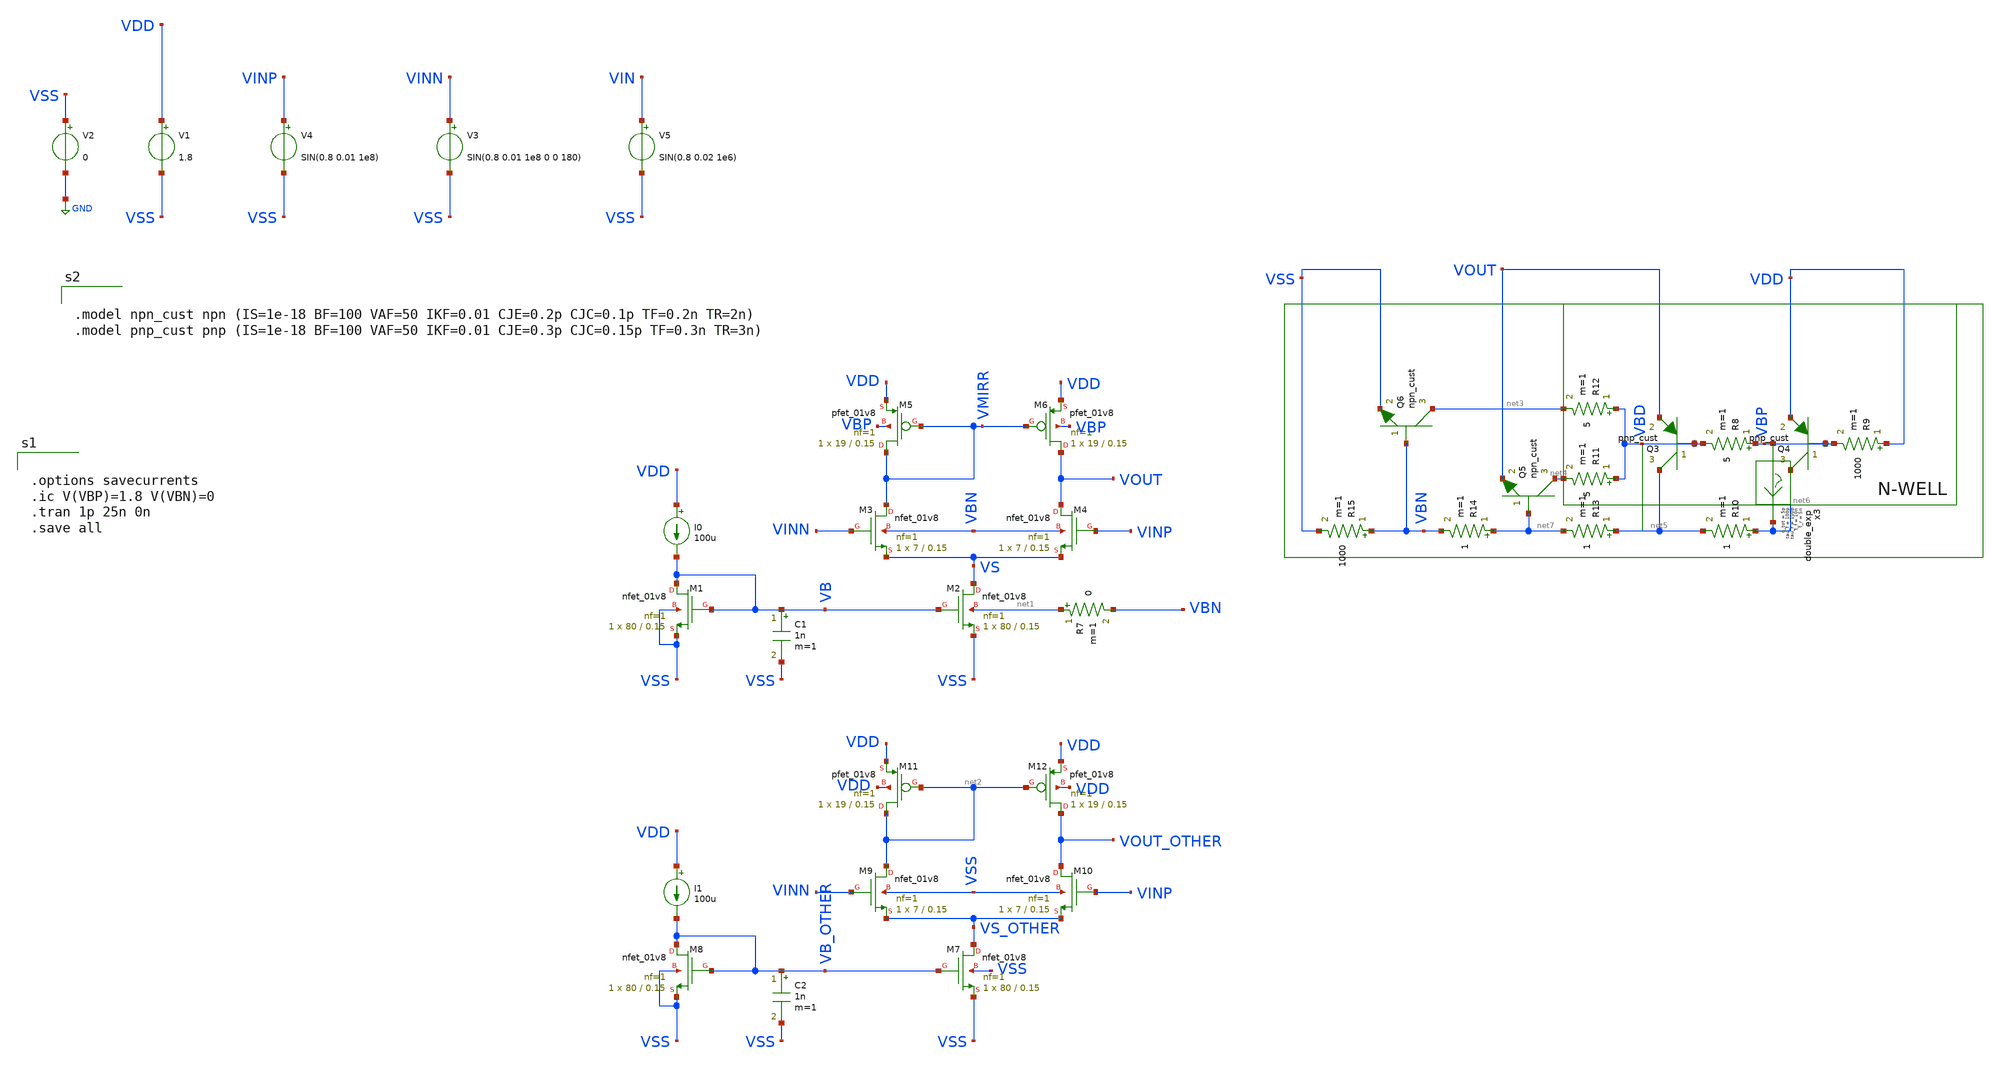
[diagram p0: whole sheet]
** sch_path: latchup/op_amp_test_complex.sch
**.subckt op_amp_test_complex
XM2 VS VB VSS net1 sky130_fd_pr__nfet_01v8 L=0.15 W=80 nf=1 ad='int((nf+1)/2) * W/nf * 0.29' as='int((nf+2)/2) * W/nf * 0.29'
+ pd='2*int((nf+1)/2) * (W/nf + 0.29)' ps='2*int((nf+2)/2) * (W/nf + 0.29)' nrd='0.29 / W' nrs='0.29 / W'
+ sa=0 sb=0 sd=0 mult=1 m=1
V1 VDD VSS 1.8
V2 VSS GND 0
XM1 VB VB VSS VSS sky130_fd_pr__nfet_01v8 L=0.15 W=80 nf=1 ad='int((nf+1)/2) * W/nf * 0.29' as='int((nf+2)/2) * W/nf * 0.29'
+ pd='2*int((nf+1)/2) * (W/nf + 0.29)' ps='2*int((nf+2)/2) * (W/nf + 0.29)' nrd='0.29 / W' nrs='0.29 / W'
+ sa=0 sb=0 sd=0 mult=1 m=1
I0 VDD VB 100u
XM3 VMIRR VINN VS VBN sky130_fd_pr__nfet_01v8 L=0.15 W=7 nf=1 ad='int((nf+1)/2) * W/nf * 0.29' as='int((nf+2)/2) * W/nf * 0.29'
+ pd='2*int((nf+1)/2) * (W/nf + 0.29)' ps='2*int((nf+2)/2) * (W/nf + 0.29)' nrd='0.29 / W' nrs='0.29 / W'
+ sa=0 sb=0 sd=0 mult=1 m=1
XM4 VOUT VINP VS VBN sky130_fd_pr__nfet_01v8 L=0.15 W=7 nf=1 ad='int((nf+1)/2) * W/nf * 0.29' as='int((nf+2)/2) * W/nf * 0.29'
+ pd='2*int((nf+1)/2) * (W/nf + 0.29)' ps='2*int((nf+2)/2) * (W/nf + 0.29)' nrd='0.29 / W' nrs='0.29 / W'
+ sa=0 sb=0 sd=0 mult=1 m=1
XM5 VMIRR VMIRR VDD VBP sky130_fd_pr__pfet_01v8 L=0.15 W=19 nf=1 ad='int((nf+1)/2) * W/nf * 0.29' as='int((nf+2)/2) * W/nf * 0.29'
+ pd='2*int((nf+1)/2) * (W/nf + 0.29)' ps='2*int((nf+2)/2) * (W/nf + 0.29)' nrd='0.29 / W' nrs='0.29 / W'
+ sa=0 sb=0 sd=0 mult=1 m=1
XM6 VOUT VMIRR VDD VBP sky130_fd_pr__pfet_01v8 L=0.15 W=19 nf=1 ad='int((nf+1)/2) * W/nf * 0.29' as='int((nf+2)/2) * W/nf * 0.29'
+ pd='2*int((nf+1)/2) * (W/nf + 0.29)' ps='2*int((nf+2)/2) * (W/nf + 0.29)' nrd='0.29 / W' nrs='0.29 / W'
+ sa=0 sb=0 sd=0 mult=1 m=1
V4 VINP VSS SIN(0.8 0.01 1e8)
V3 VINN VSS SIN(0.8 0.01 1e8 0 0 180)
C1 VB VSS 1n m=1
V5 VIN VSS SIN(0.8 0.02 1e6)
XM7 VS_OTHER VB_OTHER VSS VSS sky130_fd_pr__nfet_01v8 L=0.15 W=80 nf=1 ad='int((nf+1)/2) * W/nf * 0.29'
+ as='int((nf+2)/2) * W/nf * 0.29' pd='2*int((nf+1)/2) * (W/nf + 0.29)' ps='2*int((nf+2)/2) * (W/nf + 0.29)'
+ nrd='0.29 / W' nrs='0.29 / W' sa=0 sb=0 sd=0 mult=1 m=1
XM8 VB_OTHER VB_OTHER VSS VSS sky130_fd_pr__nfet_01v8 L=0.15 W=80 nf=1 ad='int((nf+1)/2) * W/nf * 0.29'
+ as='int((nf+2)/2) * W/nf * 0.29' pd='2*int((nf+1)/2) * (W/nf + 0.29)' ps='2*int((nf+2)/2) * (W/nf + 0.29)'
+ nrd='0.29 / W' nrs='0.29 / W' sa=0 sb=0 sd=0 mult=1 m=1
I1 VDD VB_OTHER 100u
XM9 net2 VINN VS_OTHER VSS sky130_fd_pr__nfet_01v8 L=0.15 W=7 nf=1 ad='int((nf+1)/2) * W/nf * 0.29' as='int((nf+2)/2) * W/nf * 0.29'
+ pd='2*int((nf+1)/2) * (W/nf + 0.29)' ps='2*int((nf+2)/2) * (W/nf + 0.29)' nrd='0.29 / W' nrs='0.29 / W'
+ sa=0 sb=0 sd=0 mult=1 m=1
XM10 VOUT_OTHER VINP VS_OTHER VSS sky130_fd_pr__nfet_01v8 L=0.15 W=7 nf=1 ad='int((nf+1)/2) * W/nf * 0.29'
+ as='int((nf+2)/2) * W/nf * 0.29' pd='2*int((nf+1)/2) * (W/nf + 0.29)' ps='2*int((nf+2)/2) * (W/nf + 0.29)'
+ nrd='0.29 / W' nrs='0.29 / W' sa=0 sb=0 sd=0 mult=1 m=1
XM11 net2 net2 VDD VDD sky130_fd_pr__pfet_01v8 L=0.15 W=19 nf=1 ad='int((nf+1)/2) * W/nf * 0.29' as='int((nf+2)/2) * W/nf * 0.29'
+ pd='2*int((nf+1)/2) * (W/nf + 0.29)' ps='2*int((nf+2)/2) * (W/nf + 0.29)' nrd='0.29 / W' nrs='0.29 / W'
+ sa=0 sb=0 sd=0 mult=1 m=1
XM12 VOUT_OTHER net2 VDD VDD sky130_fd_pr__pfet_01v8 L=0.15 W=19 nf=1 ad='int((nf+1)/2) * W/nf * 0.29'
+ as='int((nf+2)/2) * W/nf * 0.29' pd='2*int((nf+1)/2) * (W/nf + 0.29)' ps='2*int((nf+2)/2) * (W/nf + 0.29)'
+ nrd='0.29 / W' nrs='0.29 / W' sa=0 sb=0 sd=0 mult=1 m=1
C2 VB_OTHER VSS 1n m=1
R7 net1 VBN 0 m=1
Q3 net5 VBD VOUT pnp_cust area=1 m=1
Q4 net6 VBP VDD pnp_cust area=1 m=1
R8 VBP VBD 5 m=1
R9 VDD VBP 1000 m=1
R10 net6 net5 1 m=1
R11 VBD net4 5 m=1
R12 VBD net3 5 m=1
Q5 net4 net7 VOUT npn_cust area=1 m=1
Q6 net3 VBN VSS npn_cust area=1 m=1
R13 net5 net7 1 m=1
R14 net7 VBN 1 m=1
R15 VBN VSS 1000 m=1
x3 VBP net6 double_exp t_r=5n tau_r=100p t_f=10n tau_f=100p q_tot=5p
**** begin user architecture code


.options savecurrents
.ic V(VBP)=1.8 V(VBN)=0
.tran 1p 25n 0n
.save all



** opencircuitdesign pdks install
.lib $::SKYWATER_MODELS/sky130.lib.spice tt




.include /usr/local/share/rad_modeling_blocks/rad_modeling_blocks.spice




.model npn_cust npn (IS=1e-18 BF=100 VAF=50 IKF=0.01 CJE=0.2p CJC=0.1p TF=0.2n TR=2n)
.model pnp_cust pnp (IS=1e-18 BF=100 VAF=50 IKF=0.01 CJE=0.3p CJC=0.15p TF=0.3n TR=3n)


**** end user architecture code
**.ends

* expanding   symbol:  double_exp.sym # of pins=2
** sym_path: xschem_rad_library/double_exp.sym
** sch_path: xschem_rad_library/double_exp.sch
.subckt double_exp in out  t_r=0 t_f=0 tau_r=0 tau_f=0 q_tot=0
*.opin OUT
*.ipin IN
I1 IN OUT EXP(0 {q_tot / (t_f-t_r+tau_f-tau_r)} {t_r} {tau_r} {t_f} {tau_f})
.ends

.GLOBAL GND
.end
